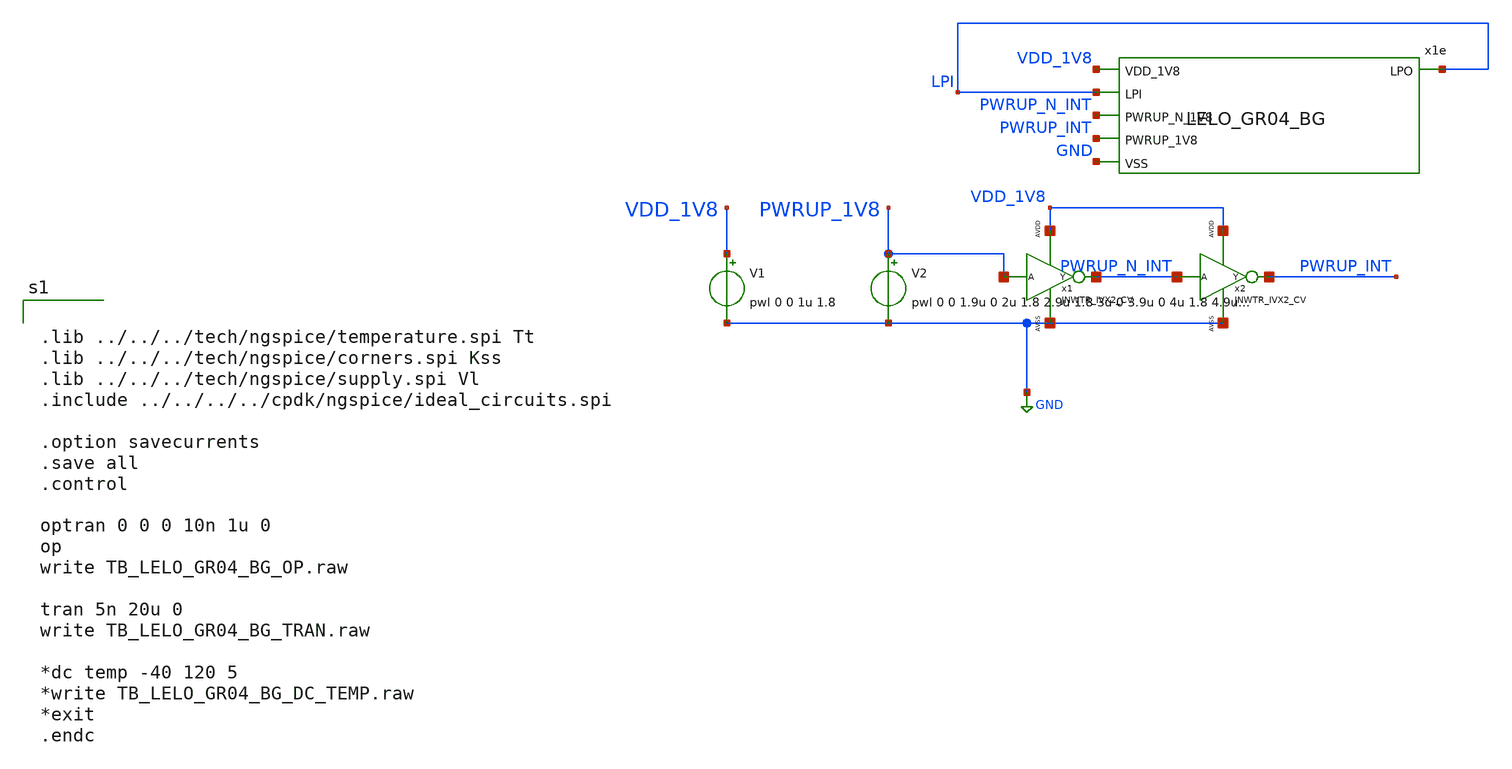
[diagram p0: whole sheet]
** sch_path: design/LELO_GR04_SKY130A/TB_LELO_GR04_BG.sch
**.subckt TB_LELO_GR04_BG
x1e VDD_1V8 LPI LPI PWRUP_N_INT PWRUP_INT GND LELO_GR04_BG
V1 VDD_1V8 GND pwl 0 0 1u 1.8
V2 PWRUP_1V8 GND pwl 0 0 1.9u 0 2u 1.8 2.9u 1.8 3u 0 3.9u 0 4u 1.8 4.9u 1.8 5u 0
x1 PWRUP_1V8 PWRUP_N_INT VDD_1V8 GND JNWTR_IVX2_CV xoffset=0 yoffset=0 angle=0 M=1
x2 PWRUP_N_INT PWRUP_INT VDD_1V8 GND JNWTR_IVX2_CV xoffset=0 yoffset=0 angle=0 M=1
**** begin user architecture code


.lib ../../../tech/ngspice/temperature.spi Tt
.lib ../../../tech/ngspice/corners.spi Kss
.lib ../../../tech/ngspice/supply.spi Vl
.include ../../../../cpdk/ngspice/ideal_circuits.spi

.option savecurrents
.save all
.control

optran 0 0 0 10n 1u 0
op
write TB_LELO_GR04_BG_OP.raw

tran 5n 20u 0
write TB_LELO_GR04_BG_TRAN.raw

*dc temp -40 120 5
*write TB_LELO_GR04_BG_DC_TEMP.raw
*exit
.endc


**** end user architecture code
**.ends
.GLOBAL GND
.end
